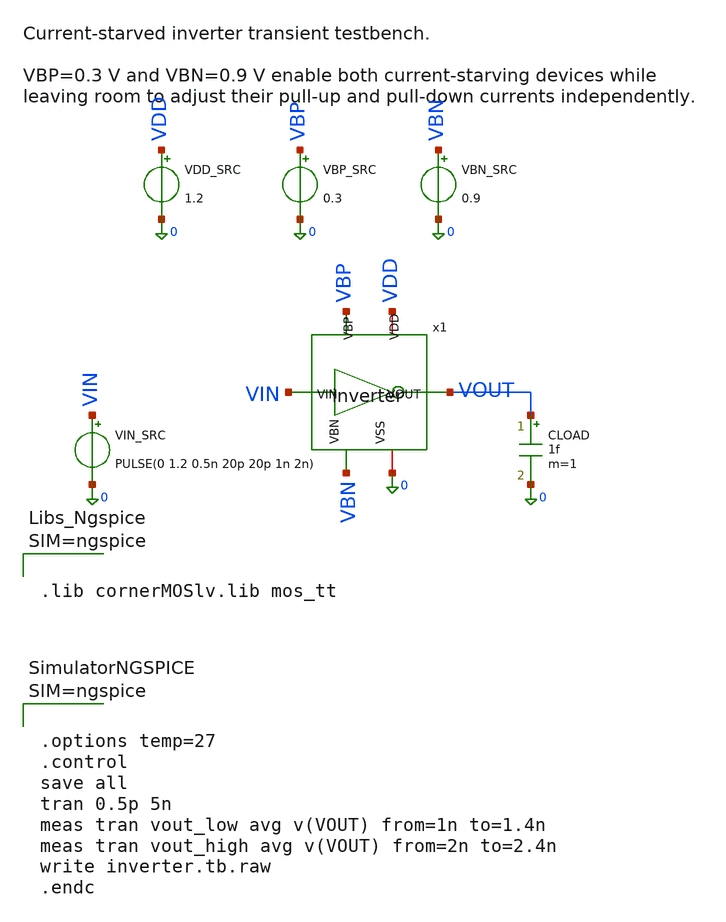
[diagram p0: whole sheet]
** sch_path: schematic/xschem/pll/testbenches/xschem/inverter.tb.sch
**.subckt inverter.tb
x1 VIN VOUT VBP VDD VBN 0 inverter
VIN_SRC VIN 0 PULSE(0 1.2 0.5n 20p 20p 1n 2n)
VDD_SRC VDD 0 1.2
VBP_SRC VBP 0 0.3
VBN_SRC VBN 0 0.9
CLOAD VOUT 0 1f m=1
**** begin user architecture code



.lib cornerMOSlv.lib mos_tt






.options temp=27
.control
save all
tran 0.5p 5n
meas tran vout_low avg v(VOUT) from=1n to=1.4n
meas tran vout_high avg v(VOUT) from=2n to=2.4n
write inverter.tb.raw
.endc



**** end user architecture code
**.ends

* expanding   symbol:  inverter.sym # of pins=6
** sym_path: schematic/xschem/pll/inverter.sym
** sch_path: schematic/xschem/pll/inverter.sch
.subckt inverter VIN VOUT VBP VDD VBN VSS
*.ipin VIN
*.ipin VBP
*.ipin VBN
*.opin VOUT
*.iopin VDD
*.iopin VSS
XM1 VDD VBP net1 VDD sg13_lv_pmos w=0.15u l=0.13u ng=1 m=1
XM2 net1 VIN VOUT VDD sg13_lv_pmos w=0.15u l=0.13u ng=1 m=1
XM3 VOUT VIN net2 VSS sg13_lv_nmos w=0.15u l=0.13u ng=1 m=1
XM4 net2 VBN VSS VSS sg13_lv_nmos w=0.15u l=0.13u ng=1 m=1
.ends

.end
